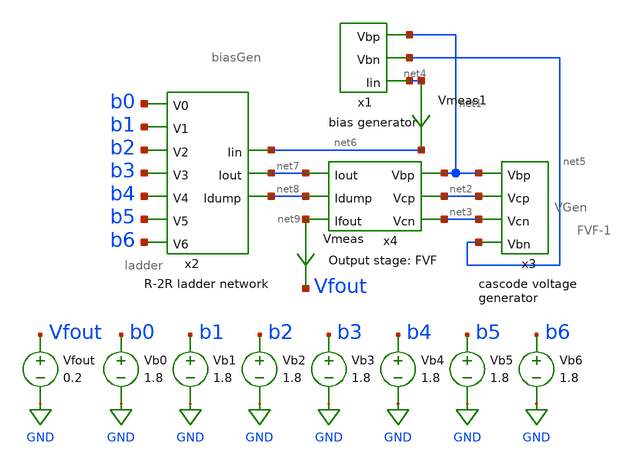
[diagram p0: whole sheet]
** sch_path: xschem/old_files/MP4-simulation-2.sch
**.subckt MP4-simulation-2
Vb0 b0 GND 1.8
x1 net1 net4 net5 biasGen
x2 net6 net8 net7 b0 b1 b2 b3 b4 b5 b6 ladder
x3 net1 net3 net2 net5 VGen
x4 net1 net2 net7 net3 net9 net8 FVF-1
Vb1 b1 GND 1.8
Vb2 b2 GND 1.8
Vb3 b3 GND 1.8
Vb4 b4 GND 1.8
Vb5 b5 GND 1.8
Vb6 b6 GND 1.8
Vfout Vfout GND 0.2
Vmeas net9 Vfout 0
.save i(vmeas)
Vmeas1 net4 net6 0
.save i(vmeas1)
**** begin user architecture code


.control
  set wr_vecnames
  set wr_singlescale
  let code = 0
  while code < 120
    if code eq 0
      let b0 = 0
    else
      let b0 = code % 2
    end
    if floor(code / 2) eq 0
      let b1 = 0
    else
      let b1 = floor(code / 2) % 2
    end
    if floor(code / 4) eq 0
      let b2 = 0
    else
      let b2 = floor(code / 4) % 2
    end
    if floor(code / 8) eq 0
      let b3 = 0
    else
      let b3 = floor(code / 8) % 2
    end
    if floor(code / 16) eq 0
      let b4 = 0
    else
      let b4 = floor(code / 16) % 2
    end
    if floor(code / 32) eq 0
      let b5 = 0
    else
      let b5 = floor(code / 32) % 2
    end
    if floor(code / 64) eq 0
      let b6 = 0
    else
      let b6 = floor(code / 64) % 2
    end
    alter Vb0 1.8*$&b0
    alter Vb1 1.8*$&b1
    alter Vb2 1.8*$&b2
    alter Vb3 1.8*$&b3
    alter Vb4 1.8*$&b4
    alter Vb5 1.8*$&b5
    alter Vb6 1.8*$&b6
    save all
    op
    wrdata ~/Documents/MP4/simulation_2.txt v(b0) v(b1) v(b2) v(b3) v(b4) v(b5) v(b6) v(Vfout)
+ i(Vmeas) i(Vmeas1)
    if code eq 0
      set appendwrite
      set wr_vecnames = FALSE
    end
    let code = code + 1
  end
  quit
.endc


.option wnflag=1
.lib ~/skywater/skywater-pdk/libraries/sky130_fd_pr_ngspice/latest/models/sky130.lib.spice tt

**** end user architecture code
**.ends

* expanding   symbol:  /home/madvlsi/DAC-VLSI/xschem/biasGen.sym # of pins=3
** sym_path: xschem/old_files/biasGen.sym
** sch_path: xschem/old_files/biasGen.sch
.subckt biasGen Vbp Iin Vbn
*.opin Iin
*.opin Vbp
*.opin Vbn
XM1 Vbn Vbn GND GND sky130_fd_pr__nfet_01v8 L=0.15 W=1 nf=1 ad='int((nf+1)/2) * W/nf * 0.29' as='int((nf+2)/2) * W/nf * 0.29'
+ pd='2*int((nf+1)/2) * (W/nf + 0.29)' ps='2*int((nf+2)/2) * (W/nf + 0.29)' nrd='0.29 / W' nrs='0.29 / W'
+ sa=0 sb=0 sd=0 mult=1 m=1
XM2 GND Vbn Vbp GND sky130_fd_pr__nfet_01v8 L=0.15 W=1 nf=1 ad='int((nf+1)/2) * W/nf * 0.29' as='int((nf+2)/2) * W/nf * 0.29'
+ pd='2*int((nf+1)/2) * (W/nf + 0.29)' ps='2*int((nf+2)/2) * (W/nf + 0.29)' nrd='0.29 / W' nrs='0.29 / W'
+ sa=0 sb=0 sd=0 mult=1 m=1
XM3 net1 net2 GND GND sky130_fd_pr__nfet_01v8 L=0.15 W=1 nf=1 ad='int((nf+1)/2) * W/nf * 0.29' as='int((nf+2)/2) * W/nf * 0.29'
+ pd='2*int((nf+1)/2) * (W/nf + 0.29)' ps='2*int((nf+2)/2) * (W/nf + 0.29)' nrd='0.29 / W' nrs='0.29 / W'
+ sa=0 sb=0 sd=0 mult=1 m=1
XM4 net3 net2 net2 GND sky130_fd_pr__nfet_01v8 L=0.15 W=8 nf=1 ad='int((nf+1)/2) * W/nf * 0.29' as='int((nf+2)/2) * W/nf * 0.29'
+ pd='2*int((nf+1)/2) * (W/nf + 0.29)' ps='2*int((nf+2)/2) * (W/nf + 0.29)' nrd='0.29 / W' nrs='0.29 / W'
+ sa=0 sb=0 sd=0 mult=1 m=1
XM5 Vbp net1 VDD VDD sky130_fd_pr__pfet_01v8 L=0.15 W=1 nf=1 ad='int((nf+1)/2) * W/nf * 0.29' as='int((nf+2)/2) * W/nf * 0.29'
+ pd='2*int((nf+1)/2) * (W/nf + 0.29)' ps='2*int((nf+2)/2) * (W/nf + 0.29)' nrd='0.29 / W' nrs='0.29 / W'
+ sa=0 sb=0 sd=0 mult=1 m=1
XM6 VDD net1 net1 VDD sky130_fd_pr__pfet_01v8 L=0.15 W=1 nf=1 ad='int((nf+1)/2) * W/nf * 0.29' as='int((nf+2)/2) * W/nf * 0.29'
+ pd='2*int((nf+1)/2) * (W/nf + 0.29)' ps='2*int((nf+2)/2) * (W/nf + 0.29)' nrd='0.29 / W' nrs='0.29 / W'
+ sa=0 sb=0 sd=0 mult=1 m=1
XM7 VDD Vbp net2 VDD sky130_fd_pr__pfet_01v8 L=0.15 W=1 nf=1 ad='int((nf+1)/2) * W/nf * 0.29' as='int((nf+2)/2) * W/nf * 0.29'
+ pd='2*int((nf+1)/2) * (W/nf + 0.29)' ps='2*int((nf+2)/2) * (W/nf + 0.29)' nrd='0.29 / W' nrs='0.29 / W'
+ sa=0 sb=0 sd=0 mult=1 m=1
XM8 Vbn Vbp VDD VDD sky130_fd_pr__pfet_01v8 L=0.15 W=1 nf=1 ad='int((nf+1)/2) * W/nf * 0.29' as='int((nf+2)/2) * W/nf * 0.29'
+ pd='2*int((nf+1)/2) * (W/nf + 0.29)' ps='2*int((nf+2)/2) * (W/nf + 0.29)' nrd='0.29 / W' nrs='0.29 / W'
+ sa=0 sb=0 sd=0 mult=1 m=1
R1 net3 GND 100k m=1
XM9 Iin Vbp VDD VDD sky130_fd_pr__pfet_01v8 L=0.15 W=1 nf=1 ad='int((nf+1)/2) * W/nf * 0.29' as='int((nf+2)/2) * W/nf * 0.29'
+ pd='2*int((nf+1)/2) * (W/nf + 0.29)' ps='2*int((nf+2)/2) * (W/nf + 0.29)' nrd='0.29 / W' nrs='0.29 / W'
+ sa=0 sb=0 sd=0 mult=1 m=1
.ends


* expanding   symbol:  /home/madvlsi/DAC-VLSI/xschem/ladder.sym # of pins=10
** sym_path: xschem/ladder.sym
** sch_path: xschem/ladder.sch
.subckt ladder Iin Idump Iout V0 V1 V2 V3 V4 V5 V6
*.ipin Iin
*.ipin V0
*.ipin V1
*.ipin V2
*.ipin V3
*.ipin V4
*.ipin V5
*.ipin V6
*.opin Idump
*.opin Iout
XM1 Iin VDD net1 GND sky130_fd_pr__nfet_01v8 L=4 W=12 nf=1 ad='int((nf+1)/2) * W/nf * 0.29' as='int((nf+2)/2) * W/nf * 0.29'
+ pd='2*int((nf+1)/2) * (W/nf + 0.29)' ps='2*int((nf+2)/2) * (W/nf + 0.29)' nrd='0.29 / W' nrs='0.29 / W'
+ sa=0 sb=0 sd=0 mult=1 m=1
XM3 Iin VDD net3 GND sky130_fd_pr__nfet_01v8 L=4 W=12 nf=1 ad='int((nf+1)/2) * W/nf * 0.29' as='int((nf+2)/2) * W/nf * 0.29'
+ pd='2*int((nf+1)/2) * (W/nf + 0.29)' ps='2*int((nf+2)/2) * (W/nf + 0.29)' nrd='0.29 / W' nrs='0.29 / W'
+ sa=0 sb=0 sd=0 mult=1 m=1
XM5 net3 VDD net4 GND sky130_fd_pr__nfet_01v8 L=4 W=12 nf=1 ad='int((nf+1)/2) * W/nf * 0.29' as='int((nf+2)/2) * W/nf * 0.29'
+ pd='2*int((nf+1)/2) * (W/nf + 0.29)' ps='2*int((nf+2)/2) * (W/nf + 0.29)' nrd='0.29 / W' nrs='0.29 / W'
+ sa=0 sb=0 sd=0 mult=1 m=1
XM7 net3 VDD net6 GND sky130_fd_pr__nfet_01v8 L=4 W=12 nf=1 ad='int((nf+1)/2) * W/nf * 0.29' as='int((nf+2)/2) * W/nf * 0.29'
+ pd='2*int((nf+1)/2) * (W/nf + 0.29)' ps='2*int((nf+2)/2) * (W/nf + 0.29)' nrd='0.29 / W' nrs='0.29 / W'
+ sa=0 sb=0 sd=0 mult=1 m=1
XM6 net4 V1 net2 GND sky130_fd_pr__nfet_01v8 L=4 W=12 nf=1 ad='int((nf+1)/2) * W/nf * 0.29' as='int((nf+2)/2) * W/nf * 0.29'
+ pd='2*int((nf+1)/2) * (W/nf + 0.29)' ps='2*int((nf+2)/2) * (W/nf + 0.29)' nrd='0.29 / W' nrs='0.29 / W'
+ sa=0 sb=0 sd=0 mult=1 m=1
XM8 net4 net18 net5 GND sky130_fd_pr__nfet_01v8 L=4 W=12 nf=1 ad='int((nf+1)/2) * W/nf * 0.29' as='int((nf+2)/2) * W/nf * 0.29'
+ pd='2*int((nf+1)/2) * (W/nf + 0.29)' ps='2*int((nf+2)/2) * (W/nf + 0.29)' nrd='0.29 / W' nrs='0.29 / W'
+ sa=0 sb=0 sd=0 mult=1 m=1
XM2 net1 V0 net2 GND sky130_fd_pr__nfet_01v8 L=4 W=12 nf=1 ad='int((nf+1)/2) * W/nf * 0.29' as='int((nf+2)/2) * W/nf * 0.29'
+ pd='2*int((nf+1)/2) * (W/nf + 0.29)' ps='2*int((nf+2)/2) * (W/nf + 0.29)' nrd='0.29 / W' nrs='0.29 / W'
+ sa=0 sb=0 sd=0 mult=1 m=1
XM4 net1 net17 net5 GND sky130_fd_pr__nfet_01v8 L=4 W=12 nf=1 ad='int((nf+1)/2) * W/nf * 0.29' as='int((nf+2)/2) * W/nf * 0.29'
+ pd='2*int((nf+1)/2) * (W/nf + 0.29)' ps='2*int((nf+2)/2) * (W/nf + 0.29)' nrd='0.29 / W' nrs='0.29 / W'
+ sa=0 sb=0 sd=0 mult=1 m=1
XM9 net6 VDD net7 GND sky130_fd_pr__nfet_01v8 L=4 W=12 nf=1 ad='int((nf+1)/2) * W/nf * 0.29' as='int((nf+2)/2) * W/nf * 0.29'
+ pd='2*int((nf+1)/2) * (W/nf + 0.29)' ps='2*int((nf+2)/2) * (W/nf + 0.29)' nrd='0.29 / W' nrs='0.29 / W'
+ sa=0 sb=0 sd=0 mult=1 m=1
XM11 net6 VDD net8 GND sky130_fd_pr__nfet_01v8 L=4 W=12 nf=1 ad='int((nf+1)/2) * W/nf * 0.29' as='int((nf+2)/2) * W/nf * 0.29'
+ pd='2*int((nf+1)/2) * (W/nf + 0.29)' ps='2*int((nf+2)/2) * (W/nf + 0.29)' nrd='0.29 / W' nrs='0.29 / W'
+ sa=0 sb=0 sd=0 mult=1 m=1
XM10 net7 V2 net2 GND sky130_fd_pr__nfet_01v8 L=4 W=12 nf=1 ad='int((nf+1)/2) * W/nf * 0.29' as='int((nf+2)/2) * W/nf * 0.29'
+ pd='2*int((nf+1)/2) * (W/nf + 0.29)' ps='2*int((nf+2)/2) * (W/nf + 0.29)' nrd='0.29 / W' nrs='0.29 / W'
+ sa=0 sb=0 sd=0 mult=1 m=1
XM12 net7 net19 net5 GND sky130_fd_pr__nfet_01v8 L=4 W=12 nf=1 ad='int((nf+1)/2) * W/nf * 0.29' as='int((nf+2)/2) * W/nf * 0.29'
+ pd='2*int((nf+1)/2) * (W/nf + 0.29)' ps='2*int((nf+2)/2) * (W/nf + 0.29)' nrd='0.29 / W' nrs='0.29 / W'
+ sa=0 sb=0 sd=0 mult=1 m=1
XM13 net8 VDD net9 GND sky130_fd_pr__nfet_01v8 L=4 W=12 nf=1 ad='int((nf+1)/2) * W/nf * 0.29' as='int((nf+2)/2) * W/nf * 0.29'
+ pd='2*int((nf+1)/2) * (W/nf + 0.29)' ps='2*int((nf+2)/2) * (W/nf + 0.29)' nrd='0.29 / W' nrs='0.29 / W'
+ sa=0 sb=0 sd=0 mult=1 m=1
XM15 net8 VDD net10 GND sky130_fd_pr__nfet_01v8 L=4 W=12 nf=1 ad='int((nf+1)/2) * W/nf * 0.29' as='int((nf+2)/2) * W/nf * 0.29'
+ pd='2*int((nf+1)/2) * (W/nf + 0.29)' ps='2*int((nf+2)/2) * (W/nf + 0.29)' nrd='0.29 / W' nrs='0.29 / W'
+ sa=0 sb=0 sd=0 mult=1 m=1
XM14 net9 V3 net2 GND sky130_fd_pr__nfet_01v8 L=4 W=12 nf=1 ad='int((nf+1)/2) * W/nf * 0.29' as='int((nf+2)/2) * W/nf * 0.29'
+ pd='2*int((nf+1)/2) * (W/nf + 0.29)' ps='2*int((nf+2)/2) * (W/nf + 0.29)' nrd='0.29 / W' nrs='0.29 / W'
+ sa=0 sb=0 sd=0 mult=1 m=1
XM16 net9 net20 net5 GND sky130_fd_pr__nfet_01v8 L=4 W=12 nf=1 ad='int((nf+1)/2) * W/nf * 0.29' as='int((nf+2)/2) * W/nf * 0.29'
+ pd='2*int((nf+1)/2) * (W/nf + 0.29)' ps='2*int((nf+2)/2) * (W/nf + 0.29)' nrd='0.29 / W' nrs='0.29 / W'
+ sa=0 sb=0 sd=0 mult=1 m=1
XM17 net10 VDD net11 GND sky130_fd_pr__nfet_01v8 L=4 W=12 nf=1 ad='int((nf+1)/2) * W/nf * 0.29' as='int((nf+2)/2) * W/nf * 0.29'
+ pd='2*int((nf+1)/2) * (W/nf + 0.29)' ps='2*int((nf+2)/2) * (W/nf + 0.29)' nrd='0.29 / W' nrs='0.29 / W'
+ sa=0 sb=0 sd=0 mult=1 m=1
XM19 net10 VDD net12 GND sky130_fd_pr__nfet_01v8 L=4 W=12 nf=1 ad='int((nf+1)/2) * W/nf * 0.29' as='int((nf+2)/2) * W/nf * 0.29'
+ pd='2*int((nf+1)/2) * (W/nf + 0.29)' ps='2*int((nf+2)/2) * (W/nf + 0.29)' nrd='0.29 / W' nrs='0.29 / W'
+ sa=0 sb=0 sd=0 mult=1 m=1
XM18 net11 V4 net2 GND sky130_fd_pr__nfet_01v8 L=4 W=12 nf=1 ad='int((nf+1)/2) * W/nf * 0.29' as='int((nf+2)/2) * W/nf * 0.29'
+ pd='2*int((nf+1)/2) * (W/nf + 0.29)' ps='2*int((nf+2)/2) * (W/nf + 0.29)' nrd='0.29 / W' nrs='0.29 / W'
+ sa=0 sb=0 sd=0 mult=1 m=1
XM20 net11 net21 net5 GND sky130_fd_pr__nfet_01v8 L=4 W=12 nf=1 ad='int((nf+1)/2) * W/nf * 0.29' as='int((nf+2)/2) * W/nf * 0.29'
+ pd='2*int((nf+1)/2) * (W/nf + 0.29)' ps='2*int((nf+2)/2) * (W/nf + 0.29)' nrd='0.29 / W' nrs='0.29 / W'
+ sa=0 sb=0 sd=0 mult=1 m=1
XM21 net12 VDD net13 GND sky130_fd_pr__nfet_01v8 L=4 W=12 nf=1 ad='int((nf+1)/2) * W/nf * 0.29' as='int((nf+2)/2) * W/nf * 0.29'
+ pd='2*int((nf+1)/2) * (W/nf + 0.29)' ps='2*int((nf+2)/2) * (W/nf + 0.29)' nrd='0.29 / W' nrs='0.29 / W'
+ sa=0 sb=0 sd=0 mult=1 m=1
XM23 net12 VDD net14 GND sky130_fd_pr__nfet_01v8 L=4 W=12 nf=1 ad='int((nf+1)/2) * W/nf * 0.29' as='int((nf+2)/2) * W/nf * 0.29'
+ pd='2*int((nf+1)/2) * (W/nf + 0.29)' ps='2*int((nf+2)/2) * (W/nf + 0.29)' nrd='0.29 / W' nrs='0.29 / W'
+ sa=0 sb=0 sd=0 mult=1 m=1
XM22 net13 V5 net2 GND sky130_fd_pr__nfet_01v8 L=4 W=12 nf=1 ad='int((nf+1)/2) * W/nf * 0.29' as='int((nf+2)/2) * W/nf * 0.29'
+ pd='2*int((nf+1)/2) * (W/nf + 0.29)' ps='2*int((nf+2)/2) * (W/nf + 0.29)' nrd='0.29 / W' nrs='0.29 / W'
+ sa=0 sb=0 sd=0 mult=1 m=1
XM24 net13 net22 net5 GND sky130_fd_pr__nfet_01v8 L=4 W=12 nf=1 ad='int((nf+1)/2) * W/nf * 0.29' as='int((nf+2)/2) * W/nf * 0.29'
+ pd='2*int((nf+1)/2) * (W/nf + 0.29)' ps='2*int((nf+2)/2) * (W/nf + 0.29)' nrd='0.29 / W' nrs='0.29 / W'
+ sa=0 sb=0 sd=0 mult=1 m=1
XM25 net14 VDD net15 GND sky130_fd_pr__nfet_01v8 L=4 W=12 nf=1 ad='int((nf+1)/2) * W/nf * 0.29' as='int((nf+2)/2) * W/nf * 0.29'
+ pd='2*int((nf+1)/2) * (W/nf + 0.29)' ps='2*int((nf+2)/2) * (W/nf + 0.29)' nrd='0.29 / W' nrs='0.29 / W'
+ sa=0 sb=0 sd=0 mult=1 m=1
XM27 net14 VDD net16 GND sky130_fd_pr__nfet_01v8 L=4 W=12 nf=1 ad='int((nf+1)/2) * W/nf * 0.29' as='int((nf+2)/2) * W/nf * 0.29'
+ pd='2*int((nf+1)/2) * (W/nf + 0.29)' ps='2*int((nf+2)/2) * (W/nf + 0.29)' nrd='0.29 / W' nrs='0.29 / W'
+ sa=0 sb=0 sd=0 mult=1 m=1
XM26 net15 V6 net2 GND sky130_fd_pr__nfet_01v8 L=4 W=12 nf=1 ad='int((nf+1)/2) * W/nf * 0.29' as='int((nf+2)/2) * W/nf * 0.29'
+ pd='2*int((nf+1)/2) * (W/nf + 0.29)' ps='2*int((nf+2)/2) * (W/nf + 0.29)' nrd='0.29 / W' nrs='0.29 / W'
+ sa=0 sb=0 sd=0 mult=1 m=1
XM28 net15 net23 net5 GND sky130_fd_pr__nfet_01v8 L=4 W=12 nf=1 ad='int((nf+1)/2) * W/nf * 0.29' as='int((nf+2)/2) * W/nf * 0.29'
+ pd='2*int((nf+1)/2) * (W/nf + 0.29)' ps='2*int((nf+2)/2) * (W/nf + 0.29)' nrd='0.29 / W' nrs='0.29 / W'
+ sa=0 sb=0 sd=0 mult=1 m=1
XM29 net16 VDD net5 GND sky130_fd_pr__nfet_01v8 L=4 W=12 nf=1 ad='int((nf+1)/2) * W/nf * 0.29' as='int((nf+2)/2) * W/nf * 0.29'
+ pd='2*int((nf+1)/2) * (W/nf + 0.29)' ps='2*int((nf+2)/2) * (W/nf + 0.29)' nrd='0.29 / W' nrs='0.29 / W'
+ sa=0 sb=0 sd=0 mult=1 m=1
XM30 GND net5 net5 GND sky130_fd_pr__nfet_01v8 L=4 W=12 nf=1 ad='int((nf+1)/2) * W/nf * 0.29' as='int((nf+2)/2) * W/nf * 0.29'
+ pd='2*int((nf+1)/2) * (W/nf + 0.29)' ps='2*int((nf+2)/2) * (W/nf + 0.29)' nrd='0.29 / W' nrs='0.29 / W'
+ sa=0 sb=0 sd=0 mult=1 m=1
XM31 GND net2 net2 GND sky130_fd_pr__nfet_01v8 L=4 W=12 nf=1 ad='int((nf+1)/2) * W/nf * 0.29' as='int((nf+2)/2) * W/nf * 0.29'
+ pd='2*int((nf+1)/2) * (W/nf + 0.29)' ps='2*int((nf+2)/2) * (W/nf + 0.29)' nrd='0.29 / W' nrs='0.29 / W'
+ sa=0 sb=0 sd=0 mult=1 m=1
XM32 Idump net5 GND GND sky130_fd_pr__nfet_01v8 L=4 W=12 nf=1 ad='int((nf+1)/2) * W/nf * 0.29' as='int((nf+2)/2) * W/nf * 0.29'
+ pd='2*int((nf+1)/2) * (W/nf + 0.29)' ps='2*int((nf+2)/2) * (W/nf + 0.29)' nrd='0.29 / W' nrs='0.29 / W'
+ sa=0 sb=0 sd=0 mult=1 m=1
XM33 Iout net2 GND GND sky130_fd_pr__nfet_01v8 L=4 W=12 nf=1 ad='int((nf+1)/2) * W/nf * 0.29' as='int((nf+2)/2) * W/nf * 0.29'
+ pd='2*int((nf+1)/2) * (W/nf + 0.29)' ps='2*int((nf+2)/2) * (W/nf + 0.29)' nrd='0.29 / W' nrs='0.29 / W'
+ sa=0 sb=0 sd=0 mult=1 m=1
x1 net17 V0 inverter
x2 net18 V1 inverter
x3 net19 V2 inverter
x4 net20 V3 inverter
x5 net21 V4 inverter
x6 net22 V5 inverter
x7 net23 V6 inverter
.ends


* expanding   symbol:  /home/madvlsi/DAC-VLSI/xschem/VGen.sym # of pins=4
** sym_path: xschem/VGen.sym
** sch_path: xschem/VGen.sch
.subckt VGen Vbp Vcn Vcp Vbn
*.opin Vcp
*.ipin Vbp
*.ipin Vbn
*.opin Vcn
XM5 net4 net4 net1 GND sky130_fd_pr__nfet_01v8 L=8 W=96 nf=1 ad='int((nf+1)/2) * W/nf * 0.29' as='int((nf+2)/2) * W/nf * 0.29'
+ pd='2*int((nf+1)/2) * (W/nf + 0.29)' ps='2*int((nf+2)/2) * (W/nf + 0.29)' nrd='0.29 / W' nrs='0.29 / W'
+ sa=0 sb=0 sd=0 mult=1 m=1
XM6 net1 net4 GND GND sky130_fd_pr__nfet_01v8 L=8 W=24 nf=1 ad='int((nf+1)/2) * W/nf * 0.29' as='int((nf+2)/2) * W/nf * 0.29'
+ pd='2*int((nf+1)/2) * (W/nf + 0.29)' ps='2*int((nf+2)/2) * (W/nf + 0.29)' nrd='0.29 / W' nrs='0.29 / W'
+ sa=0 sb=0 sd=0 mult=1 m=1
XM4 net1 Vcn Vcn GND sky130_fd_pr__nfet_01v8 L=8 W=24 nf=1 ad='int((nf+1)/2) * W/nf * 0.29' as='int((nf+2)/2) * W/nf * 0.29'
+ pd='2*int((nf+1)/2) * (W/nf + 0.29)' ps='2*int((nf+2)/2) * (W/nf + 0.29)' nrd='0.29 / W' nrs='0.29 / W'
+ sa=0 sb=0 sd=0 mult=1 m=1
XM1 VDD Vbp net4 VDD sky130_fd_pr__pfet_01v8 L=32 W=24 nf=1 ad='int((nf+1)/2) * W/nf * 0.29' as='int((nf+2)/2) * W/nf * 0.29'
+ pd='2*int((nf+1)/2) * (W/nf + 0.29)' ps='2*int((nf+2)/2) * (W/nf + 0.29)' nrd='0.29 / W' nrs='0.29 / W'
+ sa=0 sb=0 sd=0 mult=1 m=1
XM2 VDD Vbp Vcn VDD sky130_fd_pr__pfet_01v8 L=8 W=24 nf=1 ad='int((nf+1)/2) * W/nf * 0.29' as='int((nf+2)/2) * W/nf * 0.29'
+ pd='2*int((nf+1)/2) * (W/nf + 0.29)' ps='2*int((nf+2)/2) * (W/nf + 0.29)' nrd='0.29 / W' nrs='0.29 / W'
+ sa=0 sb=0 sd=0 mult=1 m=1
XM9 net3 net3 net2 VDD sky130_fd_pr__pfet_01v8 L=8 W=96 nf=1 ad='int((nf+1)/2) * W/nf * 0.29' as='int((nf+2)/2) * W/nf * 0.29'
+ pd='2*int((nf+1)/2) * (W/nf + 0.29)' ps='2*int((nf+2)/2) * (W/nf + 0.29)' nrd='0.29 / W' nrs='0.29 / W'
+ sa=0 sb=0 sd=0 mult=1 m=1
XM11 GND Vbn Vcp GND sky130_fd_pr__nfet_01v8 L=8 W=24 nf=1 ad='int((nf+1)/2) * W/nf * 0.29' as='int((nf+2)/2) * W/nf * 0.29'
+ pd='2*int((nf+1)/2) * (W/nf + 0.29)' ps='2*int((nf+2)/2) * (W/nf + 0.29)' nrd='0.29 / W' nrs='0.29 / W'
+ sa=0 sb=0 sd=0 mult=1 m=1
XM8 net2 Vcp Vcp VDD sky130_fd_pr__pfet_01v8 L=8 W=24 nf=1 ad='int((nf+1)/2) * W/nf * 0.29' as='int((nf+2)/2) * W/nf * 0.29'
+ pd='2*int((nf+1)/2) * (W/nf + 0.29)' ps='2*int((nf+2)/2) * (W/nf + 0.29)' nrd='0.29 / W' nrs='0.29 / W'
+ sa=0 sb=0 sd=0 mult=1 m=1
XM12 GND Vbn net3 GND sky130_fd_pr__nfet_01v8 L=32 W=24 nf=1 ad='int((nf+1)/2) * W/nf * 0.29' as='int((nf+2)/2) * W/nf * 0.29'
+ pd='2*int((nf+1)/2) * (W/nf + 0.29)' ps='2*int((nf+2)/2) * (W/nf + 0.29)' nrd='0.29 / W' nrs='0.29 / W'
+ sa=0 sb=0 sd=0 mult=1 m=1
XM7 net2 net3 VDD VDD sky130_fd_pr__pfet_01v8 L=8 W=24 nf=1 ad='int((nf+1)/2) * W/nf * 0.29' as='int((nf+2)/2) * W/nf * 0.29'
+ pd='2*int((nf+1)/2) * (W/nf + 0.29)' ps='2*int((nf+2)/2) * (W/nf + 0.29)' nrd='0.29 / W' nrs='0.29 / W'
+ sa=0 sb=0 sd=0 mult=1 m=1
.ends


* expanding   symbol:  /home/madvlsi/DAC-VLSI/xschem/FVF-1.sym # of pins=6
** sym_path: xschem/FVF-1.sym
** sch_path: xschem/FVF-1.sch
.subckt FVF-1 Vbp Vcp Iout Vcn Ifout Idump
*.ipin Vcn
*.ipin Iout
*.ipin Idump
*.ipin Vcp
*.ipin Vbp
*.opin Ifout
XM1 net1 Vcn Idump GND sky130_fd_pr__nfet_01v8 L=4 W=24 nf=1 ad='int((nf+1)/2) * W/nf * 0.29' as='int((nf+2)/2) * W/nf * 0.29'
+ pd='2*int((nf+1)/2) * (W/nf + 0.29)' ps='2*int((nf+2)/2) * (W/nf + 0.29)' nrd='0.29 / W' nrs='0.29 / W'
+ sa=0 sb=0 sd=0 mult=1 m=1
XM2 GND net1 Idump GND sky130_fd_pr__nfet_01v8 L=4 W=24 nf=1 ad='int((nf+1)/2) * W/nf * 0.29' as='int((nf+2)/2) * W/nf * 0.29'
+ pd='2*int((nf+1)/2) * (W/nf + 0.29)' ps='2*int((nf+2)/2) * (W/nf + 0.29)' nrd='0.29 / W' nrs='0.29 / W'
+ sa=0 sb=0 sd=0 mult=1 m=1
XM3 net2 Vcn Iout GND sky130_fd_pr__nfet_01v8 L=4 W=24 nf=1 ad='int((nf+1)/2) * W/nf * 0.29' as='int((nf+2)/2) * W/nf * 0.29'
+ pd='2*int((nf+1)/2) * (W/nf + 0.29)' ps='2*int((nf+2)/2) * (W/nf + 0.29)' nrd='0.29 / W' nrs='0.29 / W'
+ sa=0 sb=0 sd=0 mult=1 m=1
XM4 GND net2 Iout GND sky130_fd_pr__nfet_01v8 L=4 W=24 nf=1 ad='int((nf+1)/2) * W/nf * 0.29' as='int((nf+2)/2) * W/nf * 0.29'
+ pd='2*int((nf+1)/2) * (W/nf + 0.29)' ps='2*int((nf+2)/2) * (W/nf + 0.29)' nrd='0.29 / W' nrs='0.29 / W'
+ sa=0 sb=0 sd=0 mult=1 m=1
XM5 Ifout Vcn net3 GND sky130_fd_pr__nfet_01v8 L=4 W=24 nf=1 ad='int((nf+1)/2) * W/nf * 0.29' as='int((nf+2)/2) * W/nf * 0.29'
+ pd='2*int((nf+1)/2) * (W/nf + 0.29)' ps='2*int((nf+2)/2) * (W/nf + 0.29)' nrd='0.29 / W' nrs='0.29 / W'
+ sa=0 sb=0 sd=0 mult=1 m=1
XM6 net3 net2 GND GND sky130_fd_pr__nfet_01v8 L=4 W=24 nf=1 ad='int((nf+1)/2) * W/nf * 0.29' as='int((nf+2)/2) * W/nf * 0.29'
+ pd='2*int((nf+1)/2) * (W/nf + 0.29)' ps='2*int((nf+2)/2) * (W/nf + 0.29)' nrd='0.29 / W' nrs='0.29 / W'
+ sa=0 sb=0 sd=0 mult=1 m=1
XM7 net1 Vcp net4 VDD sky130_fd_pr__pfet_01v8 L=8 W=24 nf=1 ad='int((nf+1)/2) * W/nf * 0.29' as='int((nf+2)/2) * W/nf * 0.29'
+ pd='2*int((nf+1)/2) * (W/nf + 0.29)' ps='2*int((nf+2)/2) * (W/nf + 0.29)' nrd='0.29 / W' nrs='0.29 / W'
+ sa=0 sb=0 sd=0 mult=1 m=1
XM8 net2 Vcp net5 VDD sky130_fd_pr__pfet_01v8 L=8 W=24 nf=1 ad='int((nf+1)/2) * W/nf * 0.29' as='int((nf+2)/2) * W/nf * 0.29'
+ pd='2*int((nf+1)/2) * (W/nf + 0.29)' ps='2*int((nf+2)/2) * (W/nf + 0.29)' nrd='0.29 / W' nrs='0.29 / W'
+ sa=0 sb=0 sd=0 mult=1 m=1
XM9 Ifout Vcp net6 VDD sky130_fd_pr__pfet_01v8 L=8 W=24 nf=1 ad='int((nf+1)/2) * W/nf * 0.29' as='int((nf+2)/2) * W/nf * 0.29'
+ pd='2*int((nf+1)/2) * (W/nf + 0.29)' ps='2*int((nf+2)/2) * (W/nf + 0.29)' nrd='0.29 / W' nrs='0.29 / W'
+ sa=0 sb=0 sd=0 mult=1 m=1
XM15 net4 Vbp VDD VDD sky130_fd_pr__pfet_01v8 L=8 W=24 nf=1 ad='int((nf+1)/2) * W/nf * 0.29' as='int((nf+2)/2) * W/nf * 0.29'
+ pd='2*int((nf+1)/2) * (W/nf + 0.29)' ps='2*int((nf+2)/2) * (W/nf + 0.29)' nrd='0.29 / W' nrs='0.29 / W'
+ sa=0 sb=0 sd=0 mult=1 m=1
XM16 net5 Vbp VDD VDD sky130_fd_pr__pfet_01v8 L=8 W=24 nf=1 ad='int((nf+1)/2) * W/nf * 0.29' as='int((nf+2)/2) * W/nf * 0.29'
+ pd='2*int((nf+1)/2) * (W/nf + 0.29)' ps='2*int((nf+2)/2) * (W/nf + 0.29)' nrd='0.29 / W' nrs='0.29 / W'
+ sa=0 sb=0 sd=0 mult=1 m=1
XM17 net6 Vbp VDD VDD sky130_fd_pr__pfet_01v8 L=8 W=24 nf=1 ad='int((nf+1)/2) * W/nf * 0.29' as='int((nf+2)/2) * W/nf * 0.29'
+ pd='2*int((nf+1)/2) * (W/nf + 0.29)' ps='2*int((nf+2)/2) * (W/nf + 0.29)' nrd='0.29 / W' nrs='0.29 / W'
+ sa=0 sb=0 sd=0 mult=1 m=1
.ends


* expanding   symbol:  ./inverter.sym # of pins=2
** sym_path: xschem/old_files/inverter.sym
** sch_path: xschem/old_files/inverter.sch
.subckt inverter Y A
*.ipin A
*.opin Y
XM1 Y A VDD VDD sky130_fd_pr__pfet_01v8 L=0.15 W=1 nf=1 ad='int((nf+1)/2) * W/nf * 0.29' as='int((nf+2)/2) * W/nf * 0.29'
+ pd='2*int((nf+1)/2) * (W/nf + 0.29)' ps='2*int((nf+2)/2) * (W/nf + 0.29)' nrd='0.29 / W' nrs='0.29 / W'
+ sa=0 sb=0 sd=0 mult=1 m=1
XM2 Y A GND GND sky130_fd_pr__nfet_01v8 L=0.15 W=1 nf=1 ad='int((nf+1)/2) * W/nf * 0.29' as='int((nf+2)/2) * W/nf * 0.29'
+ pd='2*int((nf+1)/2) * (W/nf + 0.29)' ps='2*int((nf+2)/2) * (W/nf + 0.29)' nrd='0.29 / W' nrs='0.29 / W'
+ sa=0 sb=0 sd=0 mult=1 m=1
.ends

.GLOBAL GND
.GLOBAL VDD
.end
